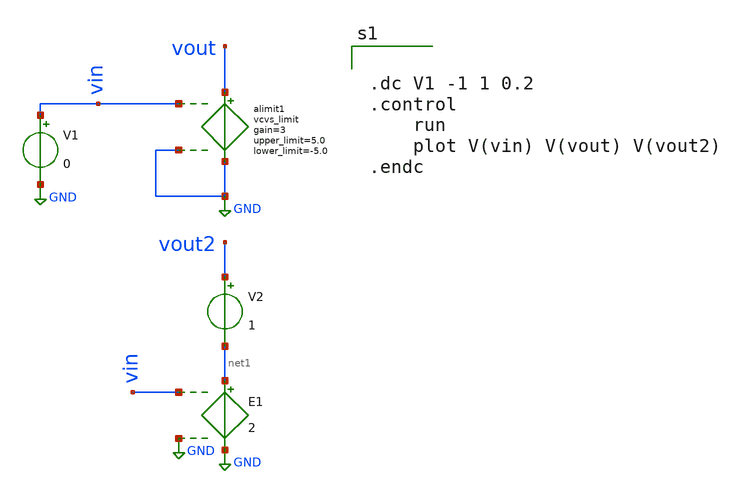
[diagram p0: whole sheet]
** sch_path: untitled.sch
**.subckt untitled
alimit1 %vd( vin GND ) %vd( vout GND ) alimit1
.model alimit1 limit ( gain=3 out_lower_limit=-5.0 out_upper_limit=5.0 )
V1 vin GND 0
E1 net1 GND vin GND 2
V2 vout2 net1 1
**** begin user architecture code


.dc V1 -1 1 0.2
.control
	run
	plot V(vin) V(vout) V(vout2)
.endc


**** end user architecture code
**.ends
.GLOBAL GND
.end
